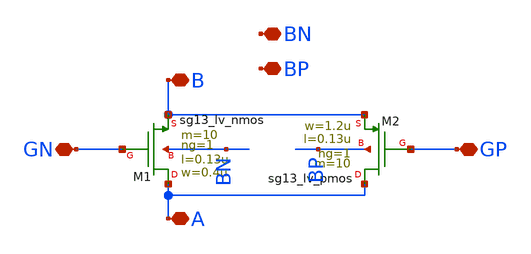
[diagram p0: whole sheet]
** sch_path: Day2/transmission_gate.sch
**.subckt transmission_gate B GN A GP BN BP
*.iopin B
*.iopin GN
*.iopin A
*.iopin GP
*.iopin BN
*.iopin BP
XM1 A GN B BN sg13_lv_nmos w=0.4u l=0.13u ng=1 m=10 mm_ok=1
XM2 A GP B BP sg13_lv_pmos w=1.2u l=0.13u ng=1 m=10 mm_ok=1
**.ends
.end
